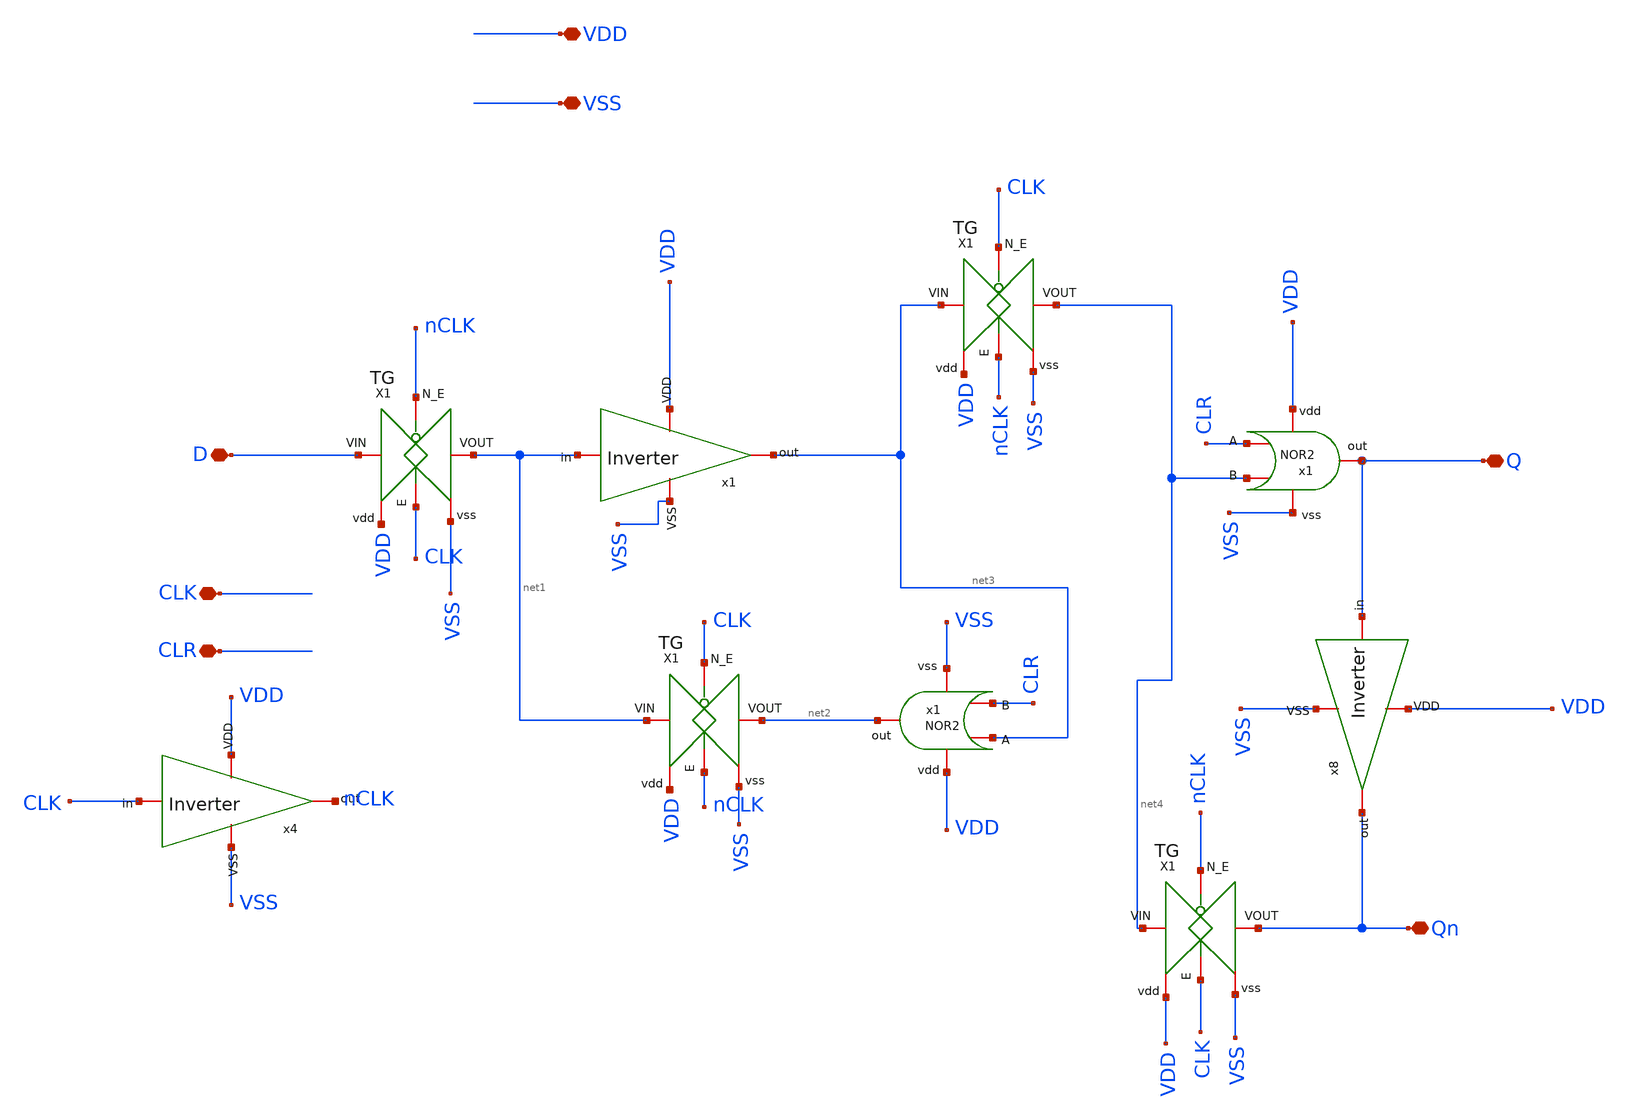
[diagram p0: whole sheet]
** sch_path: design/blocks/dffc/schematic/dffc.sch
**.subckt dffc CLK CLR Q Qn VDD VSS D
*.iopin CLK
*.iopin CLR
*.iopin Q
*.iopin Qn
*.iopin VDD
*.iopin VSS
*.iopin D
x1 VDD net3 net1 VSS inverter
x2 VDD CLR net3 net2 VSS nor2
x3 CLK net5 net1 D VDD nCLK tg
x4 VDD nCLK CLK VSS inverter
x5 nCLK VSS net2 net1 VDD CLK tg
x6 nCLK VSS net4 net3 VDD CLK tg
x7 VDD net4 CLR Q VSS nor2
x8 VDD Qn Q VSS inverter
x9 CLK VSS Qn net4 VDD nCLK tg
**.ends
.end
